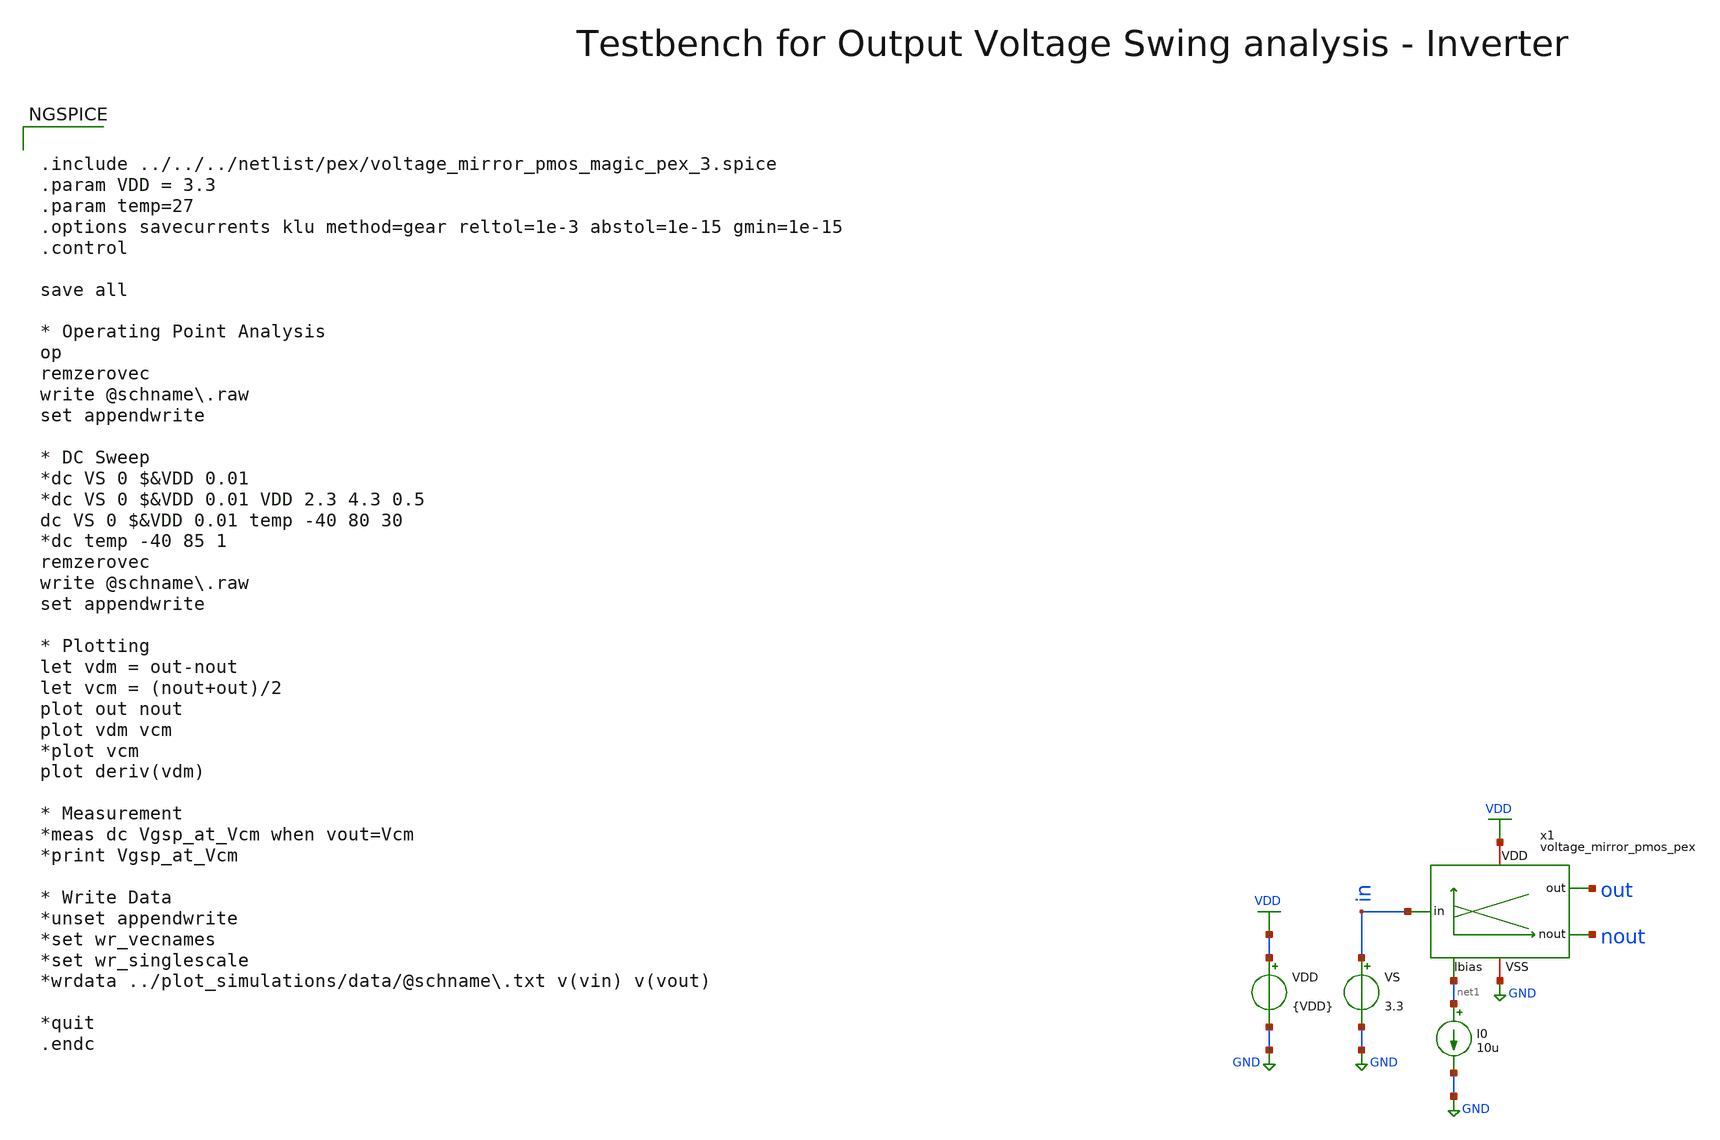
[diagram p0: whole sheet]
** sch_path: macros/heichips26_vcr/macros/switched_capacitor/testbenches/xschem/tb_voltage_mirror_pmos_pex_dc.sch
**.subckt tb_voltage_mirror_pmos_pex_dc
VDD VDD GND {VDD}
VS in GND 3.3
I0 net1 GND 10u
x1 net1 nout VDD in GND out voltage_mirror_pmos_pex
**** begin user architecture code


.include ../../../netlist/pex/voltage_mirror_pmos_magic_pex_3.spice
.param VDD = 3.3
.param temp=27
.options savecurrents klu method=gear reltol=1e-3 abstol=1e-15 gmin=1e-15
.control

save all

* Operating Point Analysis
op
remzerovec
write @schname\.raw
set appendwrite

* DC Sweep
*dc VS 0 $&VDD 0.01
*dc VS 0 $&VDD 0.01 VDD 2.3 4.3 0.5
dc VS 0 $&VDD 0.01 temp -40 80 30
*dc temp -40 85 1
remzerovec
write @schname\.raw
set appendwrite

* Plotting
let vdm = out-nout
let vcm = (nout+out)/2
plot out nout
plot vdm vcm
*plot vcm
plot deriv(vdm)

* Measurement
*meas dc Vgsp_at_Vcm when vout=Vcm
*print Vgsp_at_Vcm

* Write Data
*unset appendwrite
*set wr_vecnames
*set wr_singlescale
*wrdata ../plot_simulations/data/@schname\.txt v(vin) v(vout)

*quit
.endc



.lib cornerMOSlv.lib mos_tt
.lib cornerMOShv.lib mos_tt
.lib cornerRES.lib res_typ
.lib cornerDIO.lib dio_tt

**** end user architecture code
**.ends
.GLOBAL GND
.GLOBAL VDD
.end
